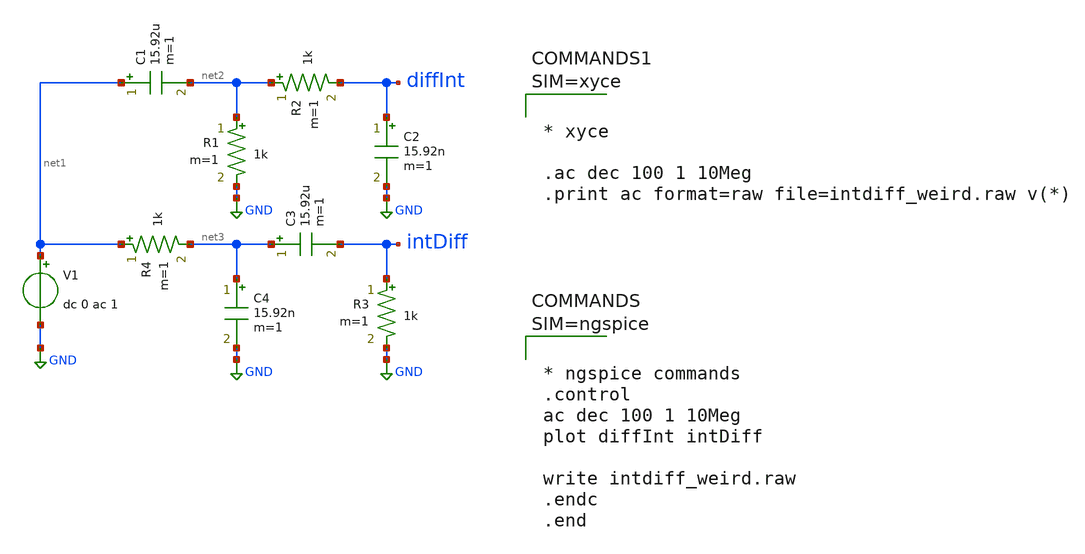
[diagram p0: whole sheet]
** sch_path: xschem/tests/dummy_tests/intdiff_weird.sch
**.subckt intdiff_weird
R1 net2 GND 1k m=1
C1 net1 net2 15.92u m=1
R2 net2 diffInt 1k m=1
C2 diffInt GND 15.92n m=1
V1 net1 GND dc 0 ac 1
R3 intDiff GND 1k m=1
C3 net3 intDiff 15.92u m=1
R4 net1 net3 1k m=1
C4 net3 GND 15.92n m=1
**** begin user architecture code



* ngspice commands
.control
ac dec 100 1 10Meg
plot diffInt intDiff

write intdiff_weird.raw
.endc
.end







**** end user architecture code
**.ends
.GLOBAL GND
.end
